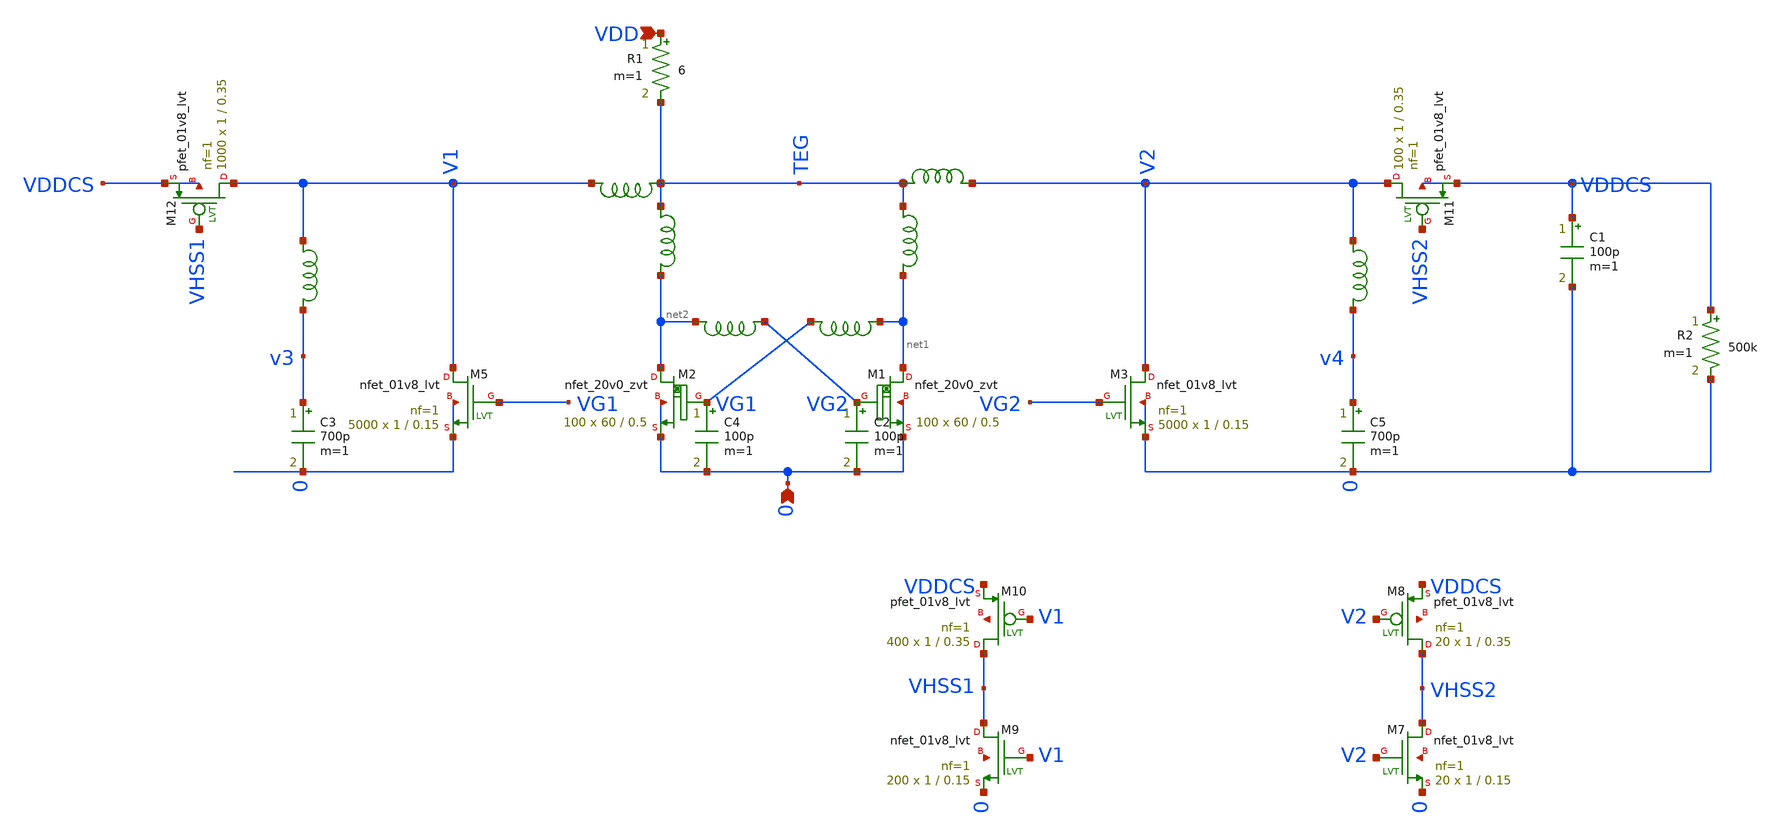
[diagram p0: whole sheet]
** sch_path: design/LELO_SVOD_SKY130A/LELO_EXSC.sch
**.subckt LELO_EXSC 0 VDD
*.ipin 0
*.ipin VDD
XM1 net1 VG2 0 0 sky130_fd_pr__nfet_20v0_zvt W=60 L=0.5 m=100
XM2 net2 VG1 0 0 sky130_fd_pr__nfet_20v0_zvt W=60 L=0.5 m=100
C1 VDDCS 0 100p m=1
C2 VG2 0 100p m=1
R1 VDD TEG 6 m=1
XM3 V2 VG2 0 0 sky130_fd_pr__nfet_01v8_lvt L=0.15 W=1 nf=1 ad='int((1 + 1)/2) * 1 / 1 * 0.29' as='int((1 + 2)/2) * 1 / 1 * 0.29'
+ pd='2*int((1 + 1)/2) * (1 / 1 + 0.29)' ps='2*int((1 + 2)/2) * (1 / 1 + 0.29)' nrd='0.29 / 1 ' nrs='0.29 / 1 '
+ sa=0 sb=0 sd=0 mult=5000 m=5000
XM5 V1 VG1 0 0 sky130_fd_pr__nfet_01v8_lvt L=0.15 W=1 nf=1 ad='int((1 + 1)/2) * 1 / 1 * 0.29' as='int((1 + 2)/2) * 1 / 1 * 0.29'
+ pd='2*int((1 + 1)/2) * (1 / 1 + 0.29)' ps='2*int((1 + 2)/2) * (1 / 1 + 0.29)' nrd='0.29 / 1 ' nrs='0.29 / 1 '
+ sa=0 sb=0 sd=0 mult=5000 m=5000
x1 VG2 net2 1812PS-564_imp
x2 net1 VG1 1812PS-564_imp
C4 VG1 0 100p m=1
x7 TEG V1 1812PS-103_imp
x8 TEG V2 1812PS-103_imp
R2 VDDCS 0 500k m=1
x3 TEG net2 1812PS-103_imp
x4 TEG net1 1812PS-103_imp
x5 V1 v3 1812PS-473_imp
C3 v3 0 700p m=1
C5 v4 0 700p m=1
x6 V2 v4 1812PS-473_imp
XM7 VHSS2 V2 0 net3 sky130_fd_pr__nfet_01v8_lvt L=0.15 W=1 nf=1 ad='int((1 + 1)/2) * 1 / 1 * 0.29' as='int((1 + 2)/2) * 1 / 1 * 0.29'
+ pd='2*int((1 + 1)/2) * (1 / 1 + 0.29)' ps='2*int((1 + 2)/2) * (1 / 1 + 0.29)' nrd='0.29 / 1 ' nrs='0.29 / 1 '
+ sa=0 sb=0 sd=0 mult=20 m=20
XM8 VHSS2 V2 VDDCS net4 sky130_fd_pr__pfet_01v8_lvt L=0.35 W=1 nf=1 ad='int((1 + 1)/2) * 1 / 1 * 0.29'
+ as='int((1 + 2)/2) * 1 / 1 * 0.29' pd='2*int((1 + 1)/2) * (1 / 1 + 0.29)' ps='2*int((1 + 2)/2) * (1 / 1 + 0.29)'
+ nrd='0.29 / 1 ' nrs='0.29 / 1 ' sa=0 sb=0 sd=0 mult=20 m=20
XM9 VHSS1 V1 0 net5 sky130_fd_pr__nfet_01v8_lvt L=0.15 W=1 nf=1 ad='int((1 + 1)/2) * 1 / 1 * 0.29' as='int((1 + 2)/2) * 1 / 1 * 0.29'
+ pd='2*int((1 + 1)/2) * (1 / 1 + 0.29)' ps='2*int((1 + 2)/2) * (1 / 1 + 0.29)' nrd='0.29 / 1 ' nrs='0.29 / 1 '
+ sa=0 sb=0 sd=0 mult=200 m=200
XM10 VHSS1 V1 VDDCS net6 sky130_fd_pr__pfet_01v8_lvt L=0.35 W=1 nf=1 ad='int((1 + 1)/2) * 1 / 1 * 0.29'
+ as='int((1 + 2)/2) * 1 / 1 * 0.29' pd='2*int((1 + 1)/2) * (1 / 1 + 0.29)' ps='2*int((1 + 2)/2) * (1 / 1 + 0.29)'
+ nrd='0.29 / 1 ' nrs='0.29 / 1 ' sa=0 sb=0 sd=0 mult=400 m=400
XM11 V2 VHSS2 VDDCS VDDCS sky130_fd_pr__pfet_01v8_lvt L=0.35 W=1 nf=1 ad='int((1 + 1)/2) * 1 / 1 * 0.29'
+ as='int((1 + 2)/2) * 1 / 1 * 0.29' pd='2*int((1 + 1)/2) * (1 / 1 + 0.29)' ps='2*int((1 + 2)/2) * (1 / 1 + 0.29)'
+ nrd='0.29 / 1 ' nrs='0.29 / 1 ' sa=0 sb=0 sd=0 mult=100 m=100
XM12 V1 VHSS1 VDDCS VDDCS sky130_fd_pr__pfet_01v8_lvt L=0.35 W=1 nf=1 ad='int((1 + 1)/2) * 1 / 1 * 0.29'
+ as='int((1 + 2)/2) * 1 / 1 * 0.29' pd='2*int((1 + 1)/2) * (1 / 1 + 0.29)' ps='2*int((1 + 2)/2) * (1 / 1 + 0.29)'
+ nrd='0.29 / 1 ' nrs='0.29 / 1 ' sa=0 sb=0 sd=0 mult=1000 m=1000
**.ends

* expanding   symbol:  LELO_SVOD_SKY130A/1812PS-564_imp.sym # of pins=2
** sym_path: design/LELO_SVOD_SKY130A/1812PS-564_imp.sym

.subckt 1812PS-564_imp port1 port2
X1 port1 port2 Model1D R1=70 R2=6.1 C= 7.71p K1=0.000001 K2=115.8 K3= 560u K4=0.000001 K5=0.000001
+ L=0 Is=0 a=0 L_Z0=0 L_EL=0 L_F0=0E6 PkZ=153558.837
.ends 1812PS-564_imp

* expanding   symbol:  LELO_SVOD_SKY130A/1812PS-103_imp.sym # of pins=2
** sym_path: design/LELO_SVOD_SKY130A/1812PS-103_imp.sym

.subckt 1812PS-103_imp port1 port2
X1 port1 port2 Model1D R1=29 R2=0.17 C= 0.28p K1=0.000001 K2=0.741 K3= 10u K4=0.0014 K5=0.0000509
+ L=0 Is=0 a=0 L_Z0=0 L_EL=0 L_F0=0E6 PkZ=7186.74953
.ends 1812PS-103_imp

* expanding   symbol:  LELO_SVOD_SKY130A/1812PS-473_imp.sym # of pins=2
** sym_path: design/LELO_SVOD_SKY130A/1812PS-473_imp.sym

.subckt 1812PS-473_imp port1 port2
X1 port1 port2 Model1D R1=30 R2=0.87 C= 0.767p K1=0.000001 K2=4.63 K3= 47u K4=0.647 K5=0.00000972
+ L=0 Is=0 a=0 L_Z0=0 L_EL=0 L_F0=0E6 PkZ=23517.1382
.ends 1812PS-473_imp
.end
